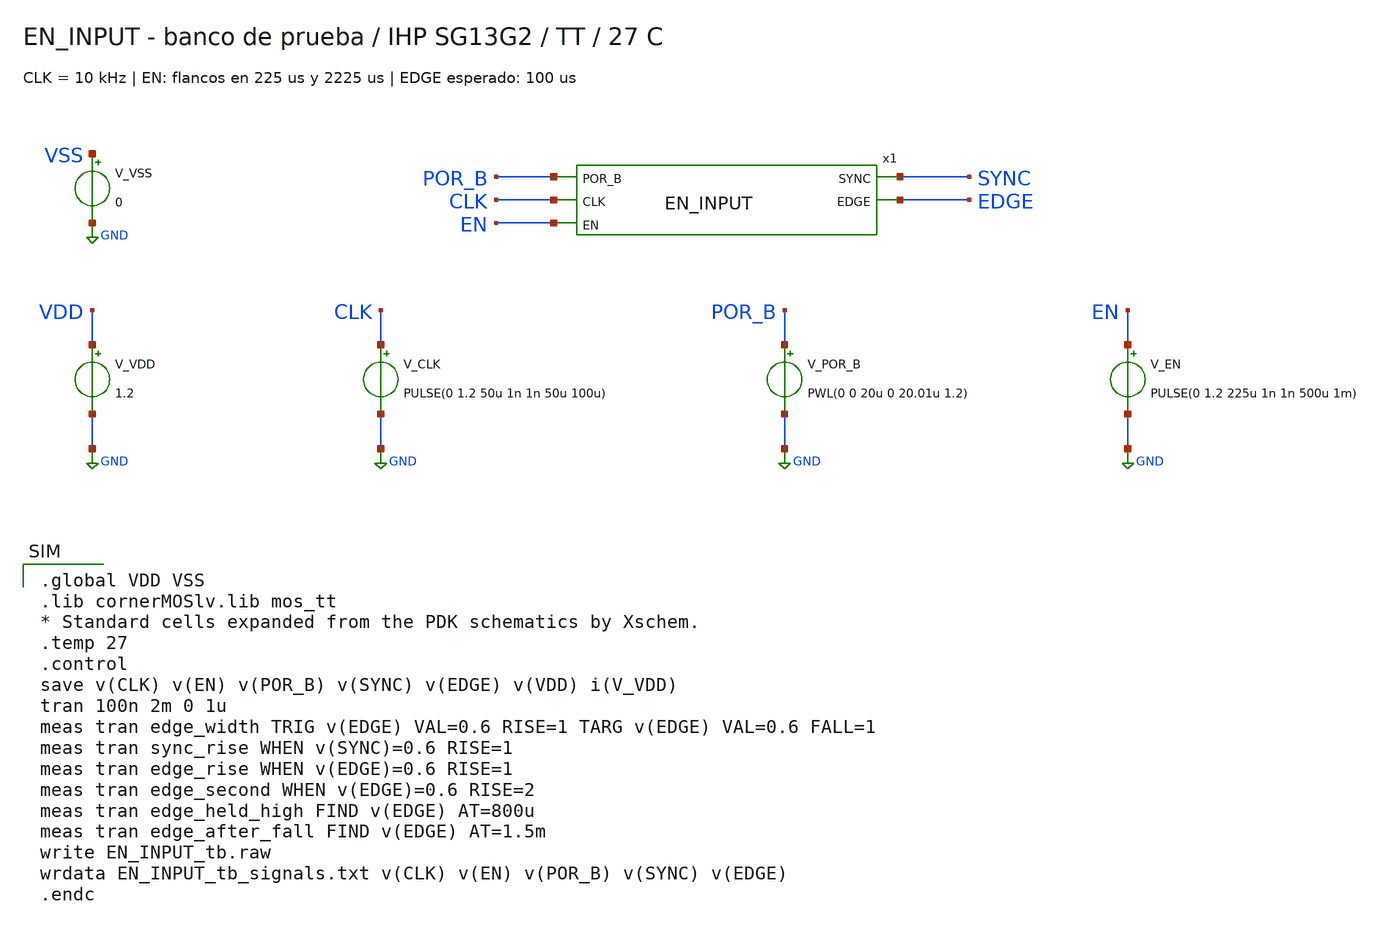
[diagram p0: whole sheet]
** sch_path: design/blocks/enable_input/schematic/EN_INPUT_tb.sch
**.subckt EN_INPUT_tb
x1 POR_B CLK SYNC EN EDGE EN_INPUT
V_VDD VDD GND 1.2
V_CLK CLK GND PULSE(0 1.2 50u 1n 1n 50u 100u)
V_POR_B POR_B GND PWL(0 0 20u 0 20.01u 1.2)
V_EN EN GND PULSE(0 1.2 225u 1n 1n 500u 1m)
V_VSS VSS GND 0
**** begin user architecture code

.global VDD VSS
.lib cornerMOSlv.lib mos_tt
* Standard cells expanded from the PDK schematics by Xschem.
.temp 27
.control
save v(CLK) v(EN) v(POR_B) v(SYNC) v(EDGE) v(VDD) i(V_VDD)
tran 100n 2m 0 1u
meas tran edge_width TRIG v(EDGE) VAL=0.6 RISE=1 TARG v(EDGE) VAL=0.6 FALL=1
meas tran sync_rise WHEN v(SYNC)=0.6 RISE=1
meas tran edge_rise WHEN v(EDGE)=0.6 RISE=1
meas tran edge_second WHEN v(EDGE)=0.6 RISE=2
meas tran edge_held_high FIND v(EDGE) AT=800u
meas tran edge_after_fall FIND v(EDGE) AT=1.5m
write EN_INPUT_tb.raw
wrdata EN_INPUT_tb_signals.txt v(CLK) v(EN) v(POR_B) v(SYNC) v(EDGE)
.endc

**** end user architecture code
**.ends

* expanding   symbol:  EN_INPUT.sym # of pins=5
** sym_path: design/blocks/enable_input/schematic/EN_INPUT.sym
** sch_path: design/blocks/enable_input/schematic/EN_INPUT.sch
.subckt EN_INPUT POR_B CLK SYNC EN EDGE
*.opin EDGE
*.opin SYNC
*.ipin EN
*.ipin POR_B
*.ipin CLK
x1 EN_META CLK EN POR_B VDD VSS sg13g2_dfrbpq_1
x2 SYNC CLK EN_META POR_B VDD VSS sg13g2_dfrbpq_1
x4 EDGE HIST_N SYNC VDD VSS sg13g2_and2_1
x3 HIST HIST_N CLK SYNC POR_B VDD VSS sg13g2_dfrbp_1
.ends


* expanding   symbol:  sg13g2_dfrbpq_1.sym # of pins=4
** sym_path: sg13g2_dfrbpq_1.sym
** sch_path: sg13g2_dfrbpq_1.sch
.subckt sg13g2_dfrbpq_1 Q CLK D RESET_B VDD VSS
*.opin Q
*.ipin CLK
*.ipin D
*.ipin RESET_B
*.iopin VDD
*.iopin VSS
XM1 Db D net10 VSS sg13_lv_nmos w=420.00n l=130.00n ng=1 m=1 mm_ok=1
XM2 net10 RESET_B VSS VSS sg13_lv_nmos w=420.00n l=130.00n ng=1 m=1 mm_ok=1
XM3 net1 clkneg net9 VSS sg13_lv_nmos w=420.00n l=130.00n ng=1 m=1 mm_ok=1
XM4 net9 net1 VSS VSS sg13_lv_nmos w=420.00n l=130.00n ng=1 m=1 mm_ok=1
XM5 net1 net1 net5 VSS sg13_lv_nmos w=420.00n l=130.00n ng=1 m=1 mm_ok=1
XM6 net5 RESET_B VSS VSS sg13_lv_nmos w=420.00n l=130.00n ng=1 m=1 mm_ok=1
XM7 net2 net1 VSS VSS sg13_lv_nmos w=740.00n l=130.00n ng=1 m=1 mm_ok=1
XM8 Q net2 VSS VSS sg13_lv_nmos w=740.00n l=130.00n ng=1 m=1 mm_ok=1
XM9 clkneg CLK VSS VSS sg13_lv_nmos w=740.00n l=130.00n ng=1 m=1 mm_ok=1
XM10 clkpos clkneg VSS VSS sg13_lv_nmos w=740.00n l=130.00n ng=1 m=1 mm_ok=1
XM11 Db clkneg net3 VSS sg13_lv_nmos w=420.00n l=130.00n ng=1 m=1 mm_ok=1
XM12 net3 clkpos net8 VSS sg13_lv_nmos w=420.00n l=130.00n ng=1 m=1 mm_ok=1
XM13 net8 net3 net4 VSS sg13_lv_nmos w=420.00n l=130.00n ng=1 m=1 mm_ok=1
XM14 net4 RESET_B VSS VSS sg13_lv_nmos w=420.00n l=130.00n ng=1 m=1 mm_ok=1
XM15 net3 net3 VSS VSS sg13_lv_nmos w=740.00n l=130.00n ng=1 m=1 mm_ok=1
XM16 net3 clkpos net1 VSS sg13_lv_nmos w=740.00n l=130.00n ng=1 m=1 mm_ok=1
XM17 Db RESET_B VDD VDD sg13_lv_pmos w=420.00n l=130.00n ng=1 m=1 mm_ok=1
XM18 Db D VDD VDD sg13_lv_pmos w=420.00n l=130.00n ng=1 m=1 mm_ok=1
XM19 net7 net1 VDD VDD sg13_lv_pmos w=420.00n l=130.00n ng=1 m=1 mm_ok=1
XM20 net1 clkpos net7 VDD sg13_lv_pmos w=420.00n l=130.00n ng=1 m=1 mm_ok=1
XM21 net1 net1 VDD VDD sg13_lv_pmos w=420.00n l=130.00n ng=1 m=1 mm_ok=1
XM22 net1 RESET_B VDD VDD sg13_lv_pmos w=420.00n l=130.00n ng=1 m=1 mm_ok=1
XM23 net2 net1 VDD VDD sg13_lv_pmos w=1.12u l=130.00n ng=1 m=1 mm_ok=1
XM24 Q net2 VDD VDD sg13_lv_pmos w=1.12u l=130.00n ng=1 m=1 mm_ok=1
XM25 clkneg CLK VDD VDD sg13_lv_pmos w=1.12u l=130.00n ng=1 m=1 mm_ok=1
XM26 clkpos clkneg VDD VDD sg13_lv_pmos w=1.12u l=130.00n ng=1 m=1 mm_ok=1
XM27 Db clkpos net3 VDD sg13_lv_pmos w=420.00n l=130.00n ng=1 m=1 mm_ok=1
XM28 net6 net3 VDD VDD sg13_lv_pmos w=420.00n l=130.00n ng=1 m=1 mm_ok=1
XM29 net3 clkneg net6 VDD sg13_lv_pmos w=420.00n l=130.00n ng=1 m=1 mm_ok=1
XM30 net3 RESET_B VDD VDD sg13_lv_pmos w=420.00n l=130.00n ng=1 m=1 mm_ok=1
XM31 net3 net3 VDD VDD sg13_lv_pmos w=1.000u l=130.00n ng=1 m=1 mm_ok=1
XM32 net3 clkneg net1 VDD sg13_lv_pmos w=1.000u l=130.00n ng=1 m=1 mm_ok=1
.ends


* expanding   symbol:  sg13g2_and2_1.sym # of pins=3
** sym_path: sg13g2_and2_1.sym
** sch_path: sg13g2_and2_1.sch
.subckt sg13g2_and2_1 X A B VDD VSS
*.ipin A
*.ipin B
*.opin X
*.iopin VDD
*.iopin VSS
XM1 net1 A net2 VSS sg13_lv_nmos w=640.00n l=130.00n ng=1 m=1 mm_ok=1
XM2 net2 B VSS VSS sg13_lv_nmos w=640.00n l=130.00n ng=1 m=1 mm_ok=1
XM3 X net1 VSS VSS sg13_lv_nmos w=740.00n l=130.00n ng=1 m=1 mm_ok=1
XM4 net1 B VDD VDD sg13_lv_pmos w=840.00n l=130.00n ng=1 m=1 mm_ok=1
XM5 net1 A VDD VDD sg13_lv_pmos w=840.00n l=130.00n ng=1 m=1 mm_ok=1
XM6 X net1 VDD VDD sg13_lv_pmos w=1.12u l=130.00n ng=1 m=1 mm_ok=1
.ends


* expanding   symbol:  sg13g2_dfrbp_1.sym # of pins=5
** sym_path: sg13g2_dfrbp_1.sym
** sch_path: sg13g2_dfrbp_1.sch
.subckt sg13g2_dfrbp_1 Q Q_N CLK D RESET_B VDD VSS
*.ipin D
*.ipin RESET_B
*.ipin CLK
*.opin Q
*.opin Q_N
*.iopin VDD
*.iopin VSS
XM1 Db D net10 VSS sg13_lv_nmos w=420.00n l=130.00n ng=1 m=1 mm_ok=1
XM2 net10 RESET_B VSS VSS sg13_lv_nmos w=420.00n l=130.00n ng=1 m=1 mm_ok=1
XM3 net1 clkneg net9 VSS sg13_lv_nmos w=420.00n l=130.00n ng=1 m=1 mm_ok=1
XM4 net9 net1 VSS VSS sg13_lv_nmos w=420.00n l=130.00n ng=1 m=1 mm_ok=1
XM5 net1 net1 net5 VSS sg13_lv_nmos w=420.00n l=130.00n ng=1 m=1 mm_ok=1
XM6 net5 RESET_B VSS VSS sg13_lv_nmos w=420.00n l=130.00n ng=1 m=1 mm_ok=1
XM7 Q_N net1 VSS VSS sg13_lv_nmos w=740.00n l=130.00n ng=1 m=1 mm_ok=1
XM8 net2 net1 VSS VSS sg13_lv_nmos w=740.00n l=130.00n ng=1 m=1 mm_ok=1
XM9 Q net2 VSS VSS sg13_lv_nmos w=740.00n l=130.00n ng=1 m=1 mm_ok=1
XM10 clkneg CLK VSS VSS sg13_lv_nmos w=740.00n l=130.00n ng=1 m=1 mm_ok=1
XM11 clkpos clkneg VSS VSS sg13_lv_nmos w=740.00n l=130.00n ng=1 m=1 mm_ok=1
XM12 Db clkneg net3 VSS sg13_lv_nmos w=420.00n l=130.00n ng=1 m=1 mm_ok=1
XM13 net3 clkpos net8 VSS sg13_lv_nmos w=420.00n l=130.00n ng=1 m=1 mm_ok=1
XM14 net8 net3 net4 VSS sg13_lv_nmos w=420.00n l=130.00n ng=1 m=1 mm_ok=1
XM15 net4 RESET_B VSS VSS sg13_lv_nmos w=420.00n l=130.00n ng=1 m=1 mm_ok=1
XM16 net3 net3 VSS VSS sg13_lv_nmos w=740.00n l=130.00n ng=1 m=1 mm_ok=1
XM17 net3 clkpos net1 VSS sg13_lv_nmos w=740.00n l=130.00n ng=1 m=1 mm_ok=1
XM18 Db RESET_B VDD VDD sg13_lv_pmos w=420.00n l=130.00n ng=1 m=1 mm_ok=1
XM19 Db D VDD VDD sg13_lv_pmos w=420.00n l=130.00n ng=1 m=1 mm_ok=1
XM20 net7 net1 VDD VDD sg13_lv_pmos w=420.00n l=130.00n ng=1 m=1 mm_ok=1
XM21 net1 clkpos net7 VDD sg13_lv_pmos w=420.00n l=130.00n ng=1 m=1 mm_ok=1
XM22 net1 net1 VDD VDD sg13_lv_pmos w=420.00n l=130.00n ng=1 m=1 mm_ok=1
XM23 net1 RESET_B VDD VDD sg13_lv_pmos w=420.00n l=130.00n ng=1 m=1 mm_ok=1
XM24 Q_N net1 VDD VDD sg13_lv_pmos w=1.12u l=130.00n ng=1 m=1 mm_ok=1
XM25 net2 net1 VDD VDD sg13_lv_pmos w=1.12u l=130.00n ng=1 m=1 mm_ok=1
XM26 Q net2 VDD VDD sg13_lv_pmos w=1.12u l=130.00n ng=1 m=1 mm_ok=1
XM27 clkneg CLK VDD VDD sg13_lv_pmos w=1.12u l=130.00n ng=1 m=1 mm_ok=1
XM28 clkpos clkneg VDD VDD sg13_lv_pmos w=1.12u l=130.00n ng=1 m=1 mm_ok=1
XM29 Db clkpos net3 VDD sg13_lv_pmos w=420.00n l=130.00n ng=1 m=1 mm_ok=1
XM30 net6 net3 VDD VDD sg13_lv_pmos w=420.00n l=130.00n ng=1 m=1 mm_ok=1
XM31 net3 clkneg net6 VDD sg13_lv_pmos w=420.00n l=130.00n ng=1 m=1 mm_ok=1
XM32 net3 RESET_B VDD VDD sg13_lv_pmos w=420.00n l=130.00n ng=1 m=1 mm_ok=1
XM33 net3 net3 VDD VDD sg13_lv_pmos w=1.000u l=130.00n ng=1 m=1 mm_ok=1
XM34 net3 clkneg net1 VDD sg13_lv_pmos w=1.000u l=130.00n ng=1 m=1 mm_ok=1
.ends

.GLOBAL GND
.end
